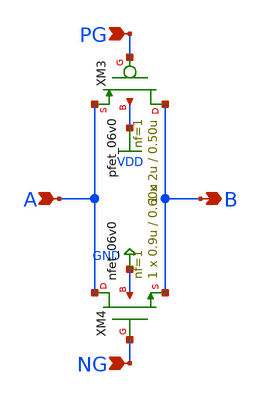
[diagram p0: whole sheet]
** sch_path: PLL/xschem/tmg.sch
**.subckt tmg B A PG NG
*.opin B
*.ipin A
*.ipin PG
*.ipin NG
XM3 B PG A VDD pfet_06v0 L=0.50u W=2u nf=1 ad='int((nf+1)/2) * W/nf * 0.18u' as='int((nf+2)/2) * W/nf * 0.18u'
+ pd='2*int((nf+1)/2) * (W/nf + 0.18u)' ps='2*int((nf+2)/2) * (W/nf + 0.18u)' nrd='0.18u / W' nrs='0.18u / W'
+ sa=0 sb=0 sd=0 m=1
XM4 A NG B GND nfet_06v0 L=0.60u W=0.9u nf=1 ad='int((nf+1)/2) * W/nf * 0.18u' as='int((nf+2)/2) * W/nf * 0.18u'
+ pd='2*int((nf+1)/2) * (W/nf + 0.18u)' ps='2*int((nf+2)/2) * (W/nf + 0.18u)' nrd='0.18u / W' nrs='0.18u / W'
+ sa=0 sb=0 sd=0 m=1
**.ends
.GLOBAL GND
.GLOBAL VDD
.end
